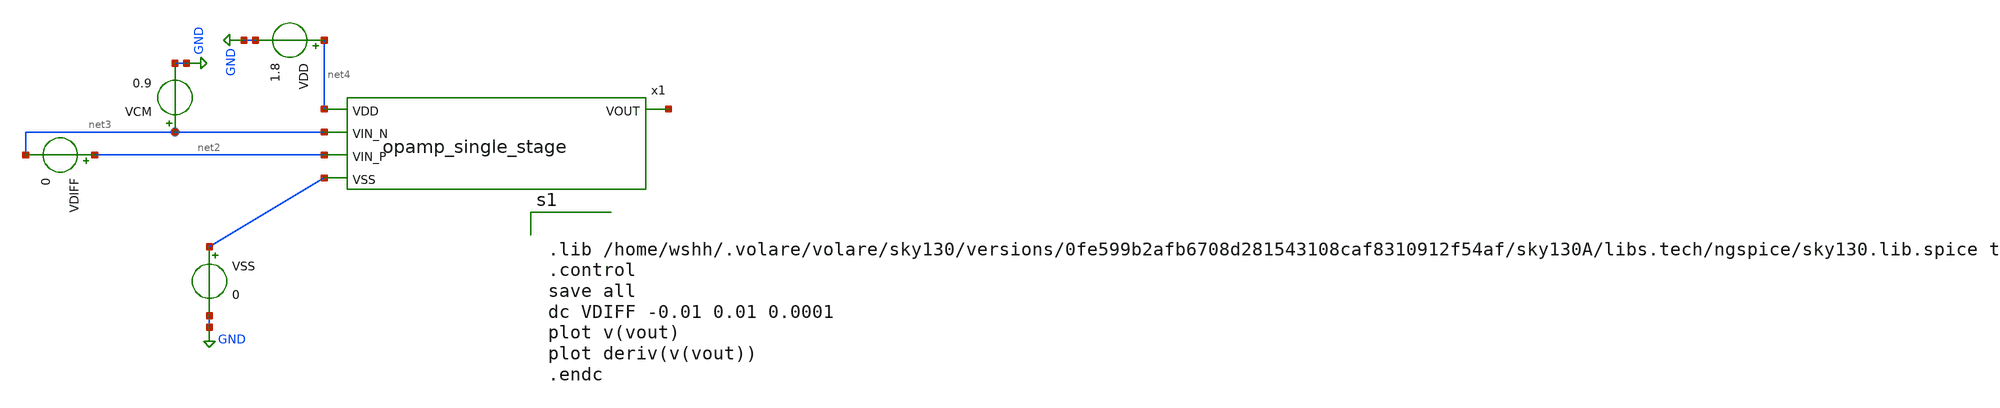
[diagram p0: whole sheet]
** sch_path: analog/build/schematic/tb_dc_analysis.sch
**.subckt tb_dc_analysis
VSS net1 GND 0
VDD net4 GND 1.8
VCM net3 GND 0.9
VDIFF net2 net3 0
x1 net5 net4 net3 net2 net1 opamp_single_stage
**** begin user architecture code


.lib /home/wshh/.volare/volare/sky130/versions/0fe599b2afb6708d281543108caf8310912f54af/sky130A/libs.tech/ngspice/sky130.lib.spice tt
.control
save all
dc VDIFF -0.01 0.01 0.0001
plot v(vout)
plot deriv(v(vout))
.endc


**** end user architecture code
**.ends

* expanding   symbol:  /home/wshh/Shiheng_Analog_Bootcamp/analog/schematics/opamp_single_stage.sym #
*+ of pins=5
** sym_path: analog/schematics/opamp_single_stage.sym
** sch_path: analog/schematics/opamp_single_stage.sch
.subckt opamp_single_stage VOUT VDD VIN_N VIN_P VSS
*.ipin VIN_P
*.ipin VIN_N
*.ipin VDD
*.ipin VSS
*.opin VOUT
XM1 net1 VIN_P net2 GND sky130_fd_pr__nfet_01v8 L=0.15 W=1 nf=1 ad='int((1 + 1)/2) * 1 / 1 * 0.29' as='int((1 + 2)/2) * 1 / 1 * 0.29'
+ pd='2*int((1 + 1)/2) * (1 / 1 + 0.29)' ps='2*int((1 + 2)/2) * (1 / 1 + 0.29)' nrd='0.29 / 1 ' nrs='0.29 / 1 '
+ sa=0 sb=0 sd=0 mult=1 m=1
XM9 VSS net3 net2 VDD sky130_fd_pr__pfet_01v8 L=0.15 W=1 nf=1 ad='int((1 + 1)/2) * 1 / 1 * 0.29' as='int((1 + 2)/2) * 1 / 1 * 0.29'
+ pd='2*int((1 + 1)/2) * (1 / 1 + 0.29)' ps='2*int((1 + 2)/2) * (1 / 1 + 0.29)' nrd='0.29 / 1 ' nrs='0.29 / 1 '
+ sa=0 sb=0 sd=0 mult=1 m=1
XM2 net2 VIN_N VOUT GND sky130_fd_pr__nfet_01v8 L=0.15 W=1 nf=1 ad='int((1 + 1)/2) * 1 / 1 * 0.29' as='int((1 + 2)/2) * 1 / 1 * 0.29'
+ pd='2*int((1 + 1)/2) * (1 / 1 + 0.29)' ps='2*int((1 + 2)/2) * (1 / 1 + 0.29)' nrd='0.29 / 1 ' nrs='0.29 / 1 '
+ sa=0 sb=0 sd=0 mult=1 m=1
XM3 VDD net1 net1 VDD sky130_fd_pr__pfet_01v8 L=0.15 W=1 nf=1 ad='int((nf+1)/2) * W/nf * 0.29' as='int((nf+2)/2) * W/nf * 0.29'
+ pd='2*int((nf+1)/2) * (W/nf + 0.29)' ps='2*int((nf+2)/2) * (W/nf + 0.29)' nrd='0.29 / W' nrs='0.29 / W'
+ sa=0 sb=0 sd=0 mult=1 m=1
XM4 VOUT net1 VDD VDD sky130_fd_pr__pfet_01v8 L=0.15 W=1 nf=1 ad='int((nf+1)/2) * W/nf * 0.29' as='int((nf+2)/2) * W/nf * 0.29'
+ pd='2*int((nf+1)/2) * (W/nf + 0.29)' ps='2*int((nf+2)/2) * (W/nf + 0.29)' nrd='0.29 / W' nrs='0.29 / W'
+ sa=0 sb=0 sd=0 mult=1 m=1
VB2 net3 net4 0.7
.ends

.GLOBAL GND
.end
